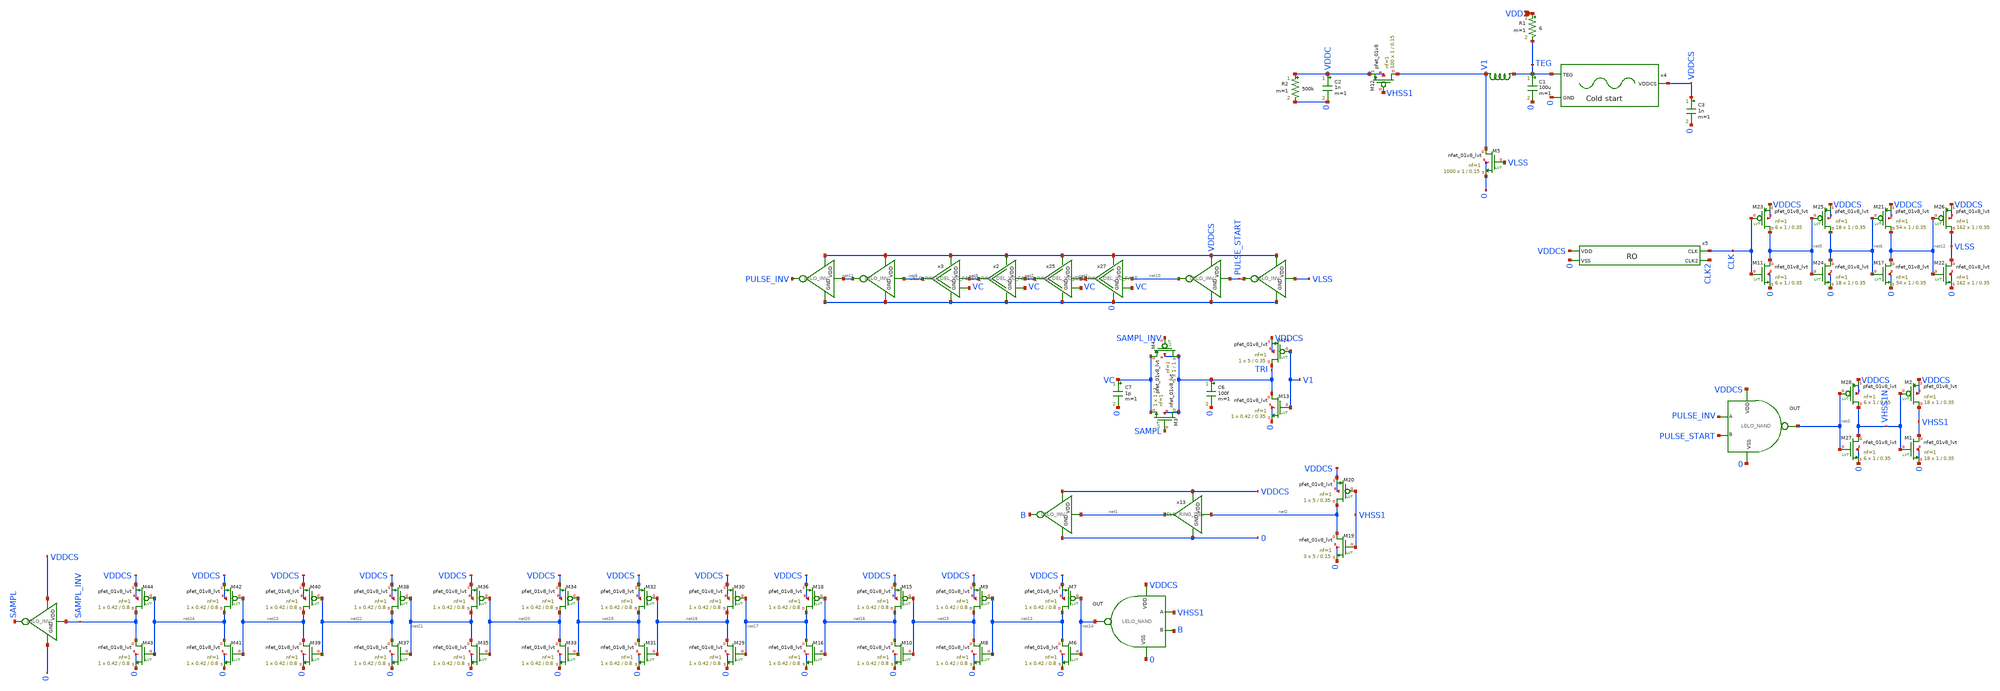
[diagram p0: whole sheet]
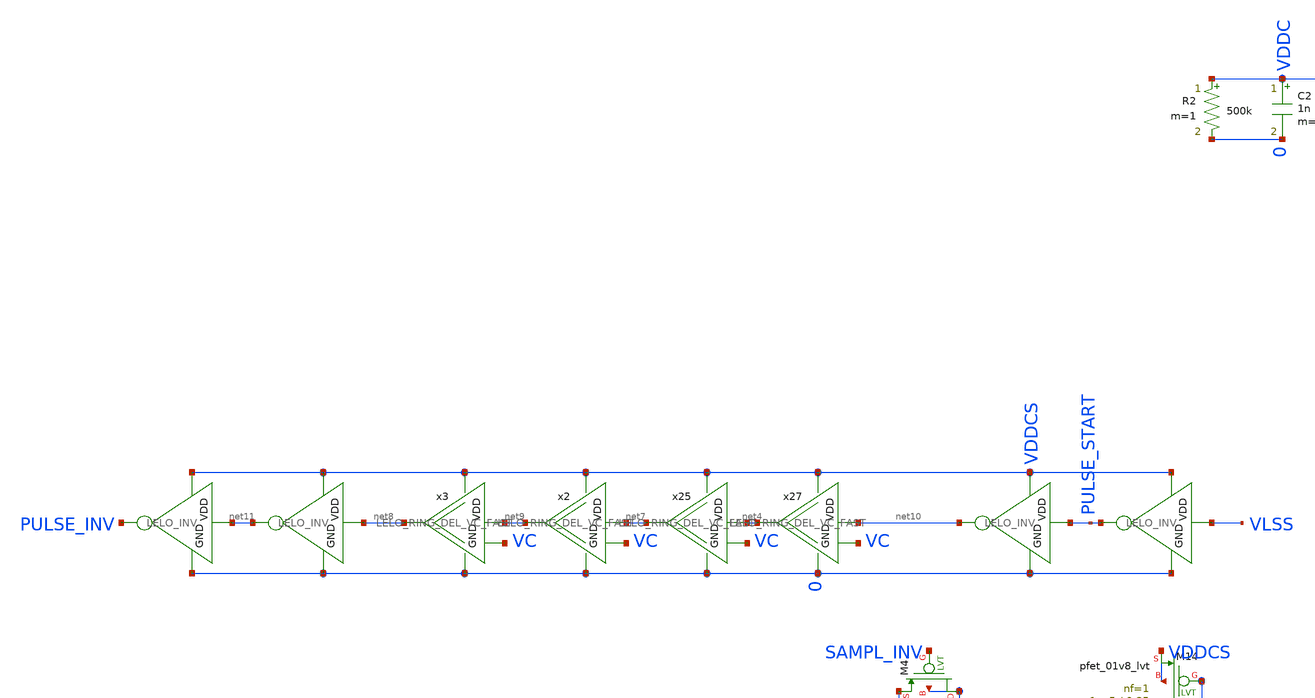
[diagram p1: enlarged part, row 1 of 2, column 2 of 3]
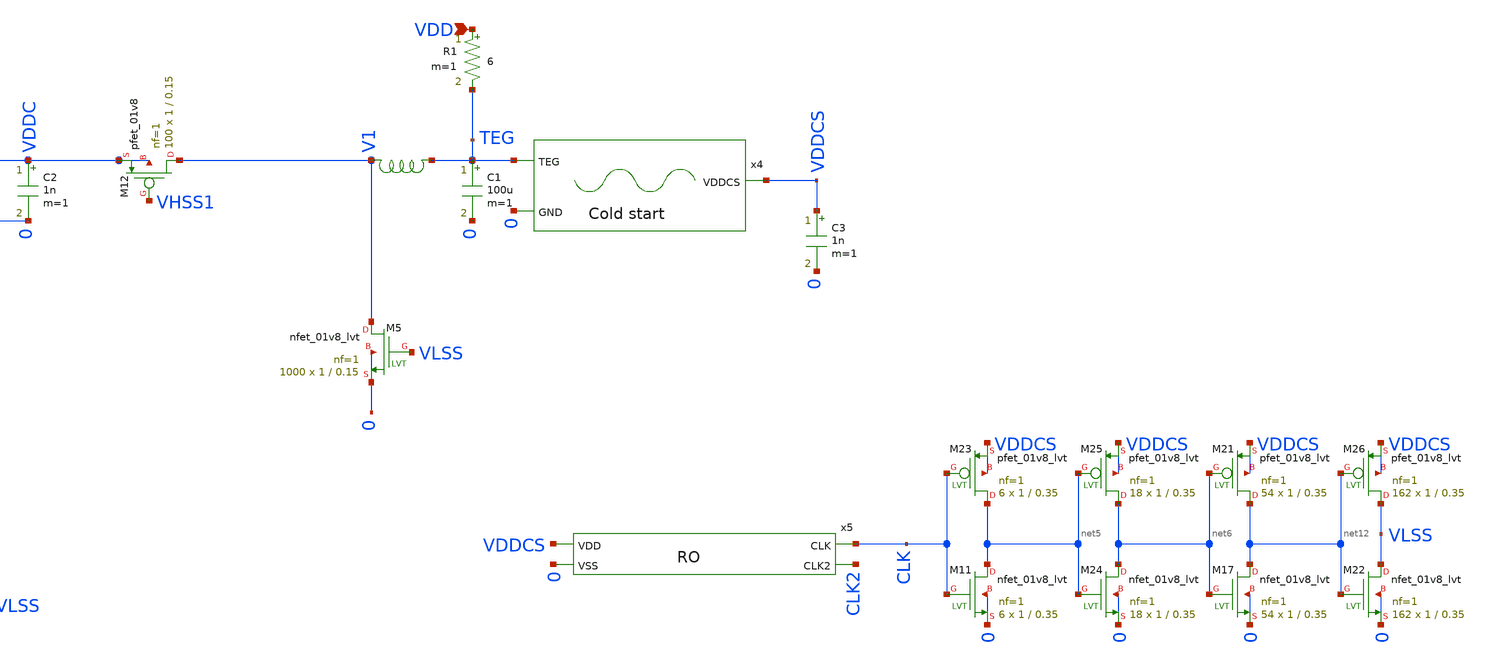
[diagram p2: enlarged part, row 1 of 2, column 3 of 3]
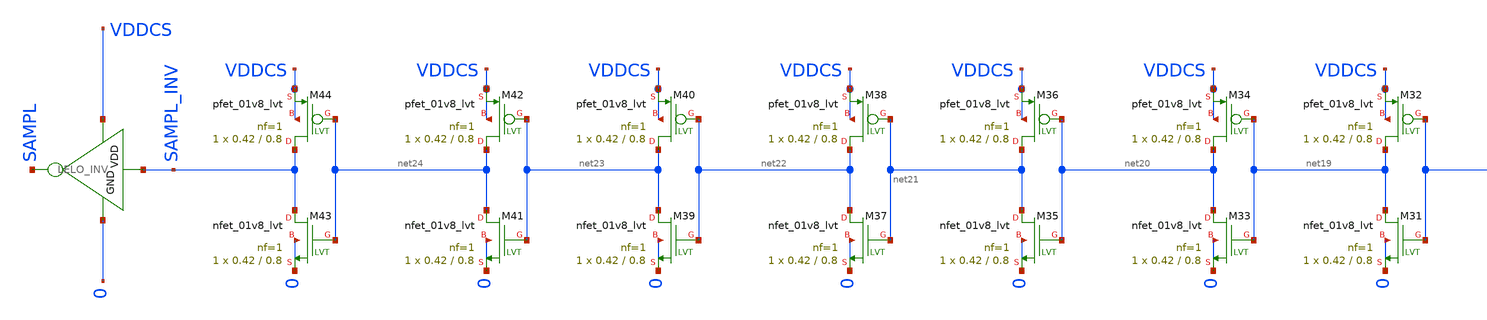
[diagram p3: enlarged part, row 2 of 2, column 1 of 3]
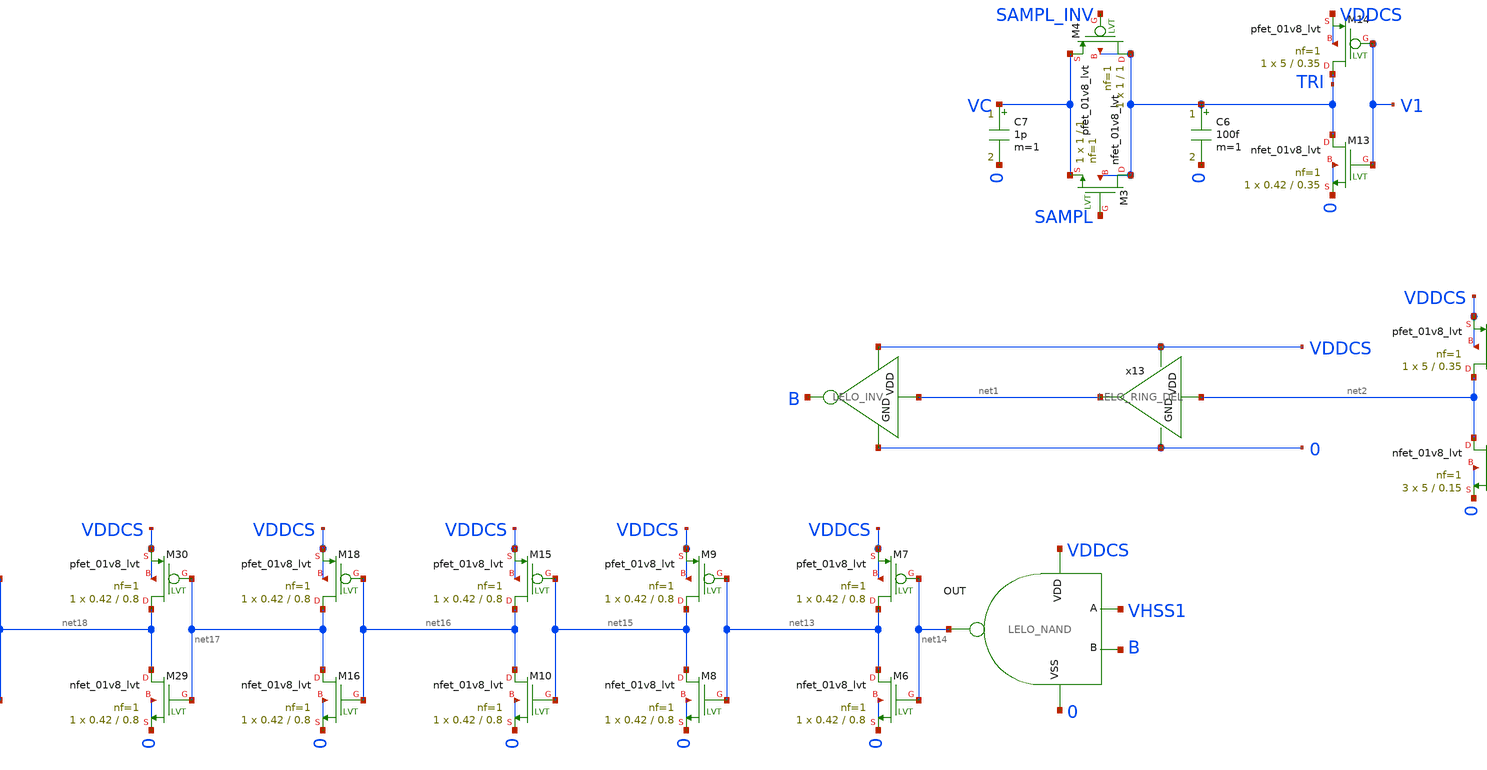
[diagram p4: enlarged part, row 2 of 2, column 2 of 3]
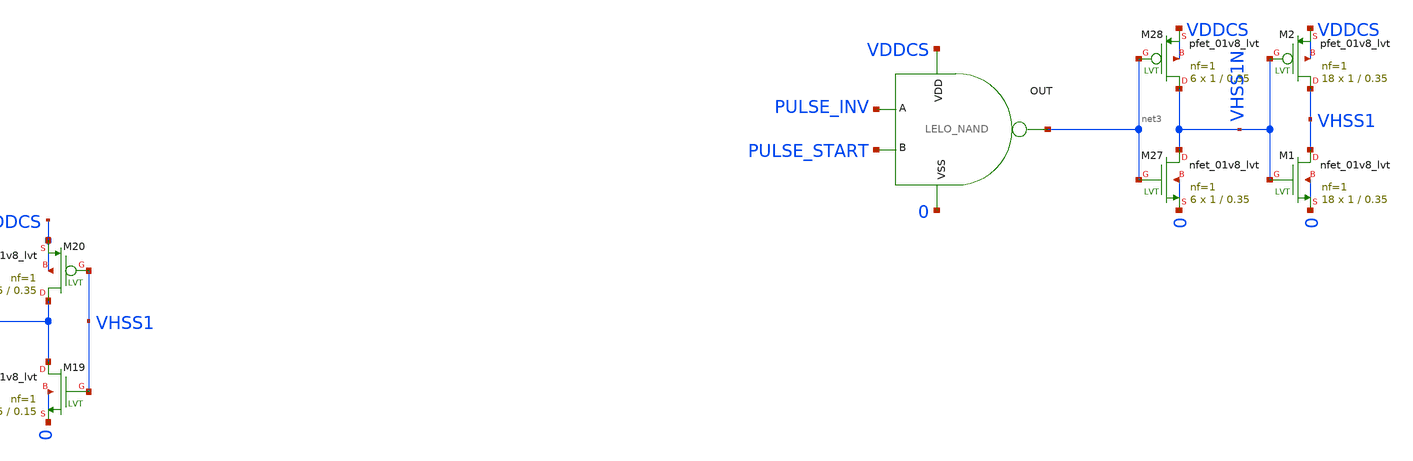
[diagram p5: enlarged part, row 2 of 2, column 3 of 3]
** sch_path: design/LELO_SVOD_SKY130A/LELO_EXSC.sch
**.subckt LELO_EXSC VDD
*.ipin VDD
R1 VDD TEG 6 m=1
XM13 TRI V1 0 0 sky130_fd_pr__nfet_01v8_lvt L=0.35 W=0.42 nf=1 ad='int((1 + 1)/2) * 0.42 / 1 * 0.29'
+ as='int((1 + 2)/2) * 0.42 / 1 * 0.29' pd='2*int((1 + 1)/2) * (0.42 / 1 + 0.29)' ps='2*int((1 + 2)/2) * (0.42 / 1 + 0.29)'
+ nrd='0.29 / 0.42 ' nrs='0.29 / 0.42 ' sa=0 sb=0 sd=0 mult=1 m=1
XM14 TRI V1 VDDCS VDDCS sky130_fd_pr__pfet_01v8_lvt L=0.35 W=5 nf=1 ad='int((1 + 1)/2) * 5 / 1 * 0.29'
+ as='int((1 + 2)/2) * 5 / 1 * 0.29' pd='2*int((1 + 1)/2) * (5 / 1 + 0.29)' ps='2*int((1 + 2)/2) * (5 / 1 + 0.29)'
+ nrd='0.29 / 5 ' nrs='0.29 / 5 ' sa=0 sb=0 sd=0 mult=1 m=1
C6 TRI 0 100f m=1
C7 VC 0 1p m=1
x13 VDDCS net2 net1 0 LELO_RING_DEL
x20 VDDCS net14 VHSS1 B 0 LELO_NAND
x22 VDDCS net1 B 0 LELO_INV
XM19 net2 VHSS1 0 0 sky130_fd_pr__nfet_01v8_lvt L=0.15 W=5 nf=1 ad='int((1 + 1)/2) * 5 / 1 * 0.29' as='int((1 + 2)/2) * 5 / 1 * 0.29'
+ pd='2*int((1 + 1)/2) * (5 / 1 + 0.29)' ps='2*int((1 + 2)/2) * (5 / 1 + 0.29)' nrd='0.29 / 5 ' nrs='0.29 / 5 '
+ sa=0 sb=0 sd=0 mult=3 m=3
XM20 net2 VHSS1 VDDCS VDDCS sky130_fd_pr__pfet_01v8_lvt L=0.35 W=5 nf=1 ad='int((1 + 1)/2) * 5 / 1 * 0.29'
+ as='int((1 + 2)/2) * 5 / 1 * 0.29' pd='2*int((1 + 1)/2) * (5 / 1 + 0.29)' ps='2*int((1 + 2)/2) * (5 / 1 + 0.29)'
+ nrd='0.29 / 5 ' nrs='0.29 / 5 ' sa=0 sb=0 sd=0 mult=1 m=1
x8 VDDCS net3 PULSE_INV PULSE_START 0 LELO_NAND
XM27 VHSS1N net3 0 0 sky130_fd_pr__nfet_01v8_lvt L=0.35 W=1 nf=1 ad='int((1 + 1)/2) * 1 / 1 * 0.29' as='int((1 + 2)/2) * 1 / 1 * 0.29'
+ pd='2*int((1 + 1)/2) * (1 / 1 + 0.29)' ps='2*int((1 + 2)/2) * (1 / 1 + 0.29)' nrd='0.29 / 1 ' nrs='0.29 / 1 '
+ sa=0 sb=0 sd=0 mult=6 m=6
XM28 VHSS1N net3 VDDCS VDDCS sky130_fd_pr__pfet_01v8_lvt L=0.35 W=1 nf=1 ad='int((1 + 1)/2) * 1 / 1 * 0.29'
+ as='int((1 + 2)/2) * 1 / 1 * 0.29' pd='2*int((1 + 1)/2) * (1 / 1 + 0.29)' ps='2*int((1 + 2)/2) * (1 / 1 + 0.29)'
+ nrd='0.29 / 1 ' nrs='0.29 / 1 ' sa=0 sb=0 sd=0 mult=6 m=6
x25 VDDCS net4 net7 0 VC LELO_RING_DEL_VC_FAST
x6 VDDCS net8 net11 0 LELO_INV
x27 VDDCS net10 net4 0 VC LELO_RING_DEL_VC_FAST
x5 VDDCS CLK CLK2 0 RO
XM11 net5 CLK 0 0 sky130_fd_pr__nfet_01v8_lvt L=0.35 W=1 nf=1 ad='int((1 + 1)/2) * 1 / 1 * 0.29' as='int((1 + 2)/2) * 1 / 1 * 0.29'
+ pd='2*int((1 + 1)/2) * (1 / 1 + 0.29)' ps='2*int((1 + 2)/2) * (1 / 1 + 0.29)' nrd='0.29 / 1 ' nrs='0.29 / 1 '
+ sa=0 sb=0 sd=0 mult=6 m=6
XM23 net5 CLK VDDCS VDDCS sky130_fd_pr__pfet_01v8_lvt L=0.35 W=1 nf=1 ad='int((1 + 1)/2) * 1 / 1 * 0.29'
+ as='int((1 + 2)/2) * 1 / 1 * 0.29' pd='2*int((1 + 1)/2) * (1 / 1 + 0.29)' ps='2*int((1 + 2)/2) * (1 / 1 + 0.29)'
+ nrd='0.29 / 1 ' nrs='0.29 / 1 ' sa=0 sb=0 sd=0 mult=6 m=6
XM24 net6 net5 0 0 sky130_fd_pr__nfet_01v8_lvt L=0.35 W=1 nf=1 ad='int((1 + 1)/2) * 1 / 1 * 0.29' as='int((1 + 2)/2) * 1 / 1 * 0.29'
+ pd='2*int((1 + 1)/2) * (1 / 1 + 0.29)' ps='2*int((1 + 2)/2) * (1 / 1 + 0.29)' nrd='0.29 / 1 ' nrs='0.29 / 1 '
+ sa=0 sb=0 sd=0 mult=18 m=18
XM25 net6 net5 VDDCS VDDCS sky130_fd_pr__pfet_01v8_lvt L=0.35 W=1 nf=1 ad='int((1 + 1)/2) * 1 / 1 * 0.29'
+ as='int((1 + 2)/2) * 1 / 1 * 0.29' pd='2*int((1 + 1)/2) * (1 / 1 + 0.29)' ps='2*int((1 + 2)/2) * (1 / 1 + 0.29)'
+ nrd='0.29 / 1 ' nrs='0.29 / 1 ' sa=0 sb=0 sd=0 mult=18 m=18
XM12 V1 VHSS1 VDDC VDDC sky130_fd_pr__pfet_01v8 L=0.15 W=1 nf=1 ad='int((1 + 1)/2) * 1 / 1 * 0.29' as='int((1 + 2)/2) * 1 / 1 * 0.29'
+ pd='2*int((1 + 1)/2) * (1 / 1 + 0.29)' ps='2*int((1 + 2)/2) * (1 / 1 + 0.29)' nrd='0.29 / 1 ' nrs='0.29 / 1 '
+ sa=0 sb=0 sd=0 mult=100 m=100
XM1 VHSS1 VHSS1N 0 0 sky130_fd_pr__nfet_01v8_lvt L=0.35 W=1 nf=1 ad='int((1 + 1)/2) * 1 / 1 * 0.29' as='int((1 + 2)/2) * 1 / 1 * 0.29'
+ pd='2*int((1 + 1)/2) * (1 / 1 + 0.29)' ps='2*int((1 + 2)/2) * (1 / 1 + 0.29)' nrd='0.29 / 1 ' nrs='0.29 / 1 '
+ sa=0 sb=0 sd=0 mult=18 m=18
XM2 VHSS1 VHSS1N VDDCS VDDCS sky130_fd_pr__pfet_01v8_lvt L=0.35 W=1 nf=1 ad='int((1 + 1)/2) * 1 / 1 * 0.29'
+ as='int((1 + 2)/2) * 1 / 1 * 0.29' pd='2*int((1 + 1)/2) * (1 / 1 + 0.29)' ps='2*int((1 + 2)/2) * (1 / 1 + 0.29)'
+ nrd='0.29 / 1 ' nrs='0.29 / 1 ' sa=0 sb=0 sd=0 mult=18 m=18
x2 VDDCS net7 net9 0 VC LELO_RING_DEL_VC_FAST
x3 VDDCS net9 net8 0 VC LELO_RING_DEL_VC_FAST
x1 VDDCS PULSE_START net10 0 LELO_INV
x16 VDDCS net11 PULSE_INV 0 LELO_INV
C1 TEG 0 100u m=1
x7 TEG V1 XGL6030-472_sat
x9 VDDCS VLSS PULSE_START 0 LELO_INV
XM5 V1 VLSS 0 0 sky130_fd_pr__nfet_01v8_lvt L=0.15 W=1 nf=1 ad='int((1 + 1)/2) * 1 / 1 * 0.29' as='int((1 + 2)/2) * 1 / 1 * 0.29'
+ pd='2*int((1 + 1)/2) * (1 / 1 + 0.29)' ps='2*int((1 + 2)/2) * (1 / 1 + 0.29)' nrd='0.29 / 1 ' nrs='0.29 / 1 '
+ sa=0 sb=0 sd=0 mult=1000 m=1000
XM17 net12 net6 0 0 sky130_fd_pr__nfet_01v8_lvt L=0.35 W=1 nf=1 ad='int((1 + 1)/2) * 1 / 1 * 0.29' as='int((1 + 2)/2) * 1 / 1 * 0.29'
+ pd='2*int((1 + 1)/2) * (1 / 1 + 0.29)' ps='2*int((1 + 2)/2) * (1 / 1 + 0.29)' nrd='0.29 / 1 ' nrs='0.29 / 1 '
+ sa=0 sb=0 sd=0 mult=54 m=54
XM21 net12 net6 VDDCS VDDCS sky130_fd_pr__pfet_01v8_lvt L=0.35 W=1 nf=1 ad='int((1 + 1)/2) * 1 / 1 * 0.29'
+ as='int((1 + 2)/2) * 1 / 1 * 0.29' pd='2*int((1 + 1)/2) * (1 / 1 + 0.29)' ps='2*int((1 + 2)/2) * (1 / 1 + 0.29)'
+ nrd='0.29 / 1 ' nrs='0.29 / 1 ' sa=0 sb=0 sd=0 mult=54 m=54
XM22 VLSS net12 0 0 sky130_fd_pr__nfet_01v8_lvt L=0.35 W=1 nf=1 ad='int((1 + 1)/2) * 1 / 1 * 0.29' as='int((1 + 2)/2) * 1 / 1 * 0.29'
+ pd='2*int((1 + 1)/2) * (1 / 1 + 0.29)' ps='2*int((1 + 2)/2) * (1 / 1 + 0.29)' nrd='0.29 / 1 ' nrs='0.29 / 1 '
+ sa=0 sb=0 sd=0 mult=162 m=162
XM26 VLSS net12 VDDCS VDDCS sky130_fd_pr__pfet_01v8_lvt L=0.35 W=1 nf=1 ad='int((1 + 1)/2) * 1 / 1 * 0.29'
+ as='int((1 + 2)/2) * 1 / 1 * 0.29' pd='2*int((1 + 1)/2) * (1 / 1 + 0.29)' ps='2*int((1 + 2)/2) * (1 / 1 + 0.29)'
+ nrd='0.29 / 1 ' nrs='0.29 / 1 ' sa=0 sb=0 sd=0 mult=162 m=162
C2 VDDC 0 1n m=1
R2 VDDC 0 500k m=1
x11 VDDCS SAMPL_INV SAMPL 0 LELO_INV
XM6 net13 net14 0 0 sky130_fd_pr__nfet_01v8_lvt L=0.8 W=0.42 nf=1 ad='int((1 + 1)/2) * 0.42 / 1 * 0.29'
+ as='int((1 + 2)/2) * 0.42 / 1 * 0.29' pd='2*int((1 + 1)/2) * (0.42 / 1 + 0.29)' ps='2*int((1 + 2)/2) * (0.42 / 1 + 0.29)'
+ nrd='0.29 / 0.42 ' nrs='0.29 / 0.42 ' sa=0 sb=0 sd=0 mult=1 m=1
XM7 net13 net14 VDDCS VDDCS sky130_fd_pr__pfet_01v8_lvt L=0.8 W=0.42 nf=1 ad='int((1 + 1)/2) * 0.42 / 1 * 0.29'
+ as='int((1 + 2)/2) * 0.42 / 1 * 0.29' pd='2*int((1 + 1)/2) * (0.42 / 1 + 0.29)' ps='2*int((1 + 2)/2) * (0.42 / 1 + 0.29)'
+ nrd='0.29 / 0.42 ' nrs='0.29 / 0.42 ' sa=0 sb=0 sd=0 mult=1 m=1
XM8 net15 net13 0 0 sky130_fd_pr__nfet_01v8_lvt L=0.8 W=0.42 nf=1 ad='int((1 + 1)/2) * 0.42 / 1 * 0.29'
+ as='int((1 + 2)/2) * 0.42 / 1 * 0.29' pd='2*int((1 + 1)/2) * (0.42 / 1 + 0.29)' ps='2*int((1 + 2)/2) * (0.42 / 1 + 0.29)'
+ nrd='0.29 / 0.42 ' nrs='0.29 / 0.42 ' sa=0 sb=0 sd=0 mult=1 m=1
XM9 net15 net13 VDDCS VDDCS sky130_fd_pr__pfet_01v8_lvt L=0.8 W=0.42 nf=1 ad='int((1 + 1)/2) * 0.42 / 1 * 0.29'
+ as='int((1 + 2)/2) * 0.42 / 1 * 0.29' pd='2*int((1 + 1)/2) * (0.42 / 1 + 0.29)' ps='2*int((1 + 2)/2) * (0.42 / 1 + 0.29)'
+ nrd='0.29 / 0.42 ' nrs='0.29 / 0.42 ' sa=0 sb=0 sd=0 mult=1 m=1
XM10 net16 net15 0 0 sky130_fd_pr__nfet_01v8_lvt L=0.8 W=0.42 nf=1 ad='int((1 + 1)/2) * 0.42 / 1 * 0.29'
+ as='int((1 + 2)/2) * 0.42 / 1 * 0.29' pd='2*int((1 + 1)/2) * (0.42 / 1 + 0.29)' ps='2*int((1 + 2)/2) * (0.42 / 1 + 0.29)'
+ nrd='0.29 / 0.42 ' nrs='0.29 / 0.42 ' sa=0 sb=0 sd=0 mult=1 m=1
XM15 net16 net15 VDDCS VDDCS sky130_fd_pr__pfet_01v8_lvt L=0.8 W=0.42 nf=1 ad='int((1 + 1)/2) * 0.42 / 1 * 0.29'
+ as='int((1 + 2)/2) * 0.42 / 1 * 0.29' pd='2*int((1 + 1)/2) * (0.42 / 1 + 0.29)' ps='2*int((1 + 2)/2) * (0.42 / 1 + 0.29)'
+ nrd='0.29 / 0.42 ' nrs='0.29 / 0.42 ' sa=0 sb=0 sd=0 mult=1 m=1
XM16 net17 net16 0 0 sky130_fd_pr__nfet_01v8_lvt L=0.8 W=0.42 nf=1 ad='int((1 + 1)/2) * 0.42 / 1 * 0.29'
+ as='int((1 + 2)/2) * 0.42 / 1 * 0.29' pd='2*int((1 + 1)/2) * (0.42 / 1 + 0.29)' ps='2*int((1 + 2)/2) * (0.42 / 1 + 0.29)'
+ nrd='0.29 / 0.42 ' nrs='0.29 / 0.42 ' sa=0 sb=0 sd=0 mult=1 m=1
XM18 net17 net16 VDDCS VDDCS sky130_fd_pr__pfet_01v8_lvt L=0.8 W=0.42 nf=1 ad='int((1 + 1)/2) * 0.42 / 1 * 0.29'
+ as='int((1 + 2)/2) * 0.42 / 1 * 0.29' pd='2*int((1 + 1)/2) * (0.42 / 1 + 0.29)' ps='2*int((1 + 2)/2) * (0.42 / 1 + 0.29)'
+ nrd='0.29 / 0.42 ' nrs='0.29 / 0.42 ' sa=0 sb=0 sd=0 mult=1 m=1
XM29 net18 net17 0 0 sky130_fd_pr__nfet_01v8_lvt L=0.8 W=0.42 nf=1 ad='int((1 + 1)/2) * 0.42 / 1 * 0.29'
+ as='int((1 + 2)/2) * 0.42 / 1 * 0.29' pd='2*int((1 + 1)/2) * (0.42 / 1 + 0.29)' ps='2*int((1 + 2)/2) * (0.42 / 1 + 0.29)'
+ nrd='0.29 / 0.42 ' nrs='0.29 / 0.42 ' sa=0 sb=0 sd=0 mult=1 m=1
XM30 net18 net17 VDDCS VDDCS sky130_fd_pr__pfet_01v8_lvt L=0.8 W=0.42 nf=1 ad='int((1 + 1)/2) * 0.42 / 1 * 0.29'
+ as='int((1 + 2)/2) * 0.42 / 1 * 0.29' pd='2*int((1 + 1)/2) * (0.42 / 1 + 0.29)' ps='2*int((1 + 2)/2) * (0.42 / 1 + 0.29)'
+ nrd='0.29 / 0.42 ' nrs='0.29 / 0.42 ' sa=0 sb=0 sd=0 mult=1 m=1
XM31 net19 net18 0 0 sky130_fd_pr__nfet_01v8_lvt L=0.8 W=0.42 nf=1 ad='int((1 + 1)/2) * 0.42 / 1 * 0.29'
+ as='int((1 + 2)/2) * 0.42 / 1 * 0.29' pd='2*int((1 + 1)/2) * (0.42 / 1 + 0.29)' ps='2*int((1 + 2)/2) * (0.42 / 1 + 0.29)'
+ nrd='0.29 / 0.42 ' nrs='0.29 / 0.42 ' sa=0 sb=0 sd=0 mult=1 m=1
XM32 net19 net18 VDDCS VDDCS sky130_fd_pr__pfet_01v8_lvt L=0.8 W=0.42 nf=1 ad='int((1 + 1)/2) * 0.42 / 1 * 0.29'
+ as='int((1 + 2)/2) * 0.42 / 1 * 0.29' pd='2*int((1 + 1)/2) * (0.42 / 1 + 0.29)' ps='2*int((1 + 2)/2) * (0.42 / 1 + 0.29)'
+ nrd='0.29 / 0.42 ' nrs='0.29 / 0.42 ' sa=0 sb=0 sd=0 mult=1 m=1
XM33 net20 net19 0 0 sky130_fd_pr__nfet_01v8_lvt L=0.8 W=0.42 nf=1 ad='int((1 + 1)/2) * 0.42 / 1 * 0.29'
+ as='int((1 + 2)/2) * 0.42 / 1 * 0.29' pd='2*int((1 + 1)/2) * (0.42 / 1 + 0.29)' ps='2*int((1 + 2)/2) * (0.42 / 1 + 0.29)'
+ nrd='0.29 / 0.42 ' nrs='0.29 / 0.42 ' sa=0 sb=0 sd=0 mult=1 m=1
XM34 net20 net19 VDDCS VDDCS sky130_fd_pr__pfet_01v8_lvt L=0.8 W=0.42 nf=1 ad='int((1 + 1)/2) * 0.42 / 1 * 0.29'
+ as='int((1 + 2)/2) * 0.42 / 1 * 0.29' pd='2*int((1 + 1)/2) * (0.42 / 1 + 0.29)' ps='2*int((1 + 2)/2) * (0.42 / 1 + 0.29)'
+ nrd='0.29 / 0.42 ' nrs='0.29 / 0.42 ' sa=0 sb=0 sd=0 mult=1 m=1
XM35 net21 net20 0 0 sky130_fd_pr__nfet_01v8_lvt L=0.8 W=0.42 nf=1 ad='int((1 + 1)/2) * 0.42 / 1 * 0.29'
+ as='int((1 + 2)/2) * 0.42 / 1 * 0.29' pd='2*int((1 + 1)/2) * (0.42 / 1 + 0.29)' ps='2*int((1 + 2)/2) * (0.42 / 1 + 0.29)'
+ nrd='0.29 / 0.42 ' nrs='0.29 / 0.42 ' sa=0 sb=0 sd=0 mult=1 m=1
XM36 net21 net20 VDDCS VDDCS sky130_fd_pr__pfet_01v8_lvt L=0.8 W=0.42 nf=1 ad='int((1 + 1)/2) * 0.42 / 1 * 0.29'
+ as='int((1 + 2)/2) * 0.42 / 1 * 0.29' pd='2*int((1 + 1)/2) * (0.42 / 1 + 0.29)' ps='2*int((1 + 2)/2) * (0.42 / 1 + 0.29)'
+ nrd='0.29 / 0.42 ' nrs='0.29 / 0.42 ' sa=0 sb=0 sd=0 mult=1 m=1
XM37 net22 net21 0 0 sky130_fd_pr__nfet_01v8_lvt L=0.8 W=0.42 nf=1 ad='int((1 + 1)/2) * 0.42 / 1 * 0.29'
+ as='int((1 + 2)/2) * 0.42 / 1 * 0.29' pd='2*int((1 + 1)/2) * (0.42 / 1 + 0.29)' ps='2*int((1 + 2)/2) * (0.42 / 1 + 0.29)'
+ nrd='0.29 / 0.42 ' nrs='0.29 / 0.42 ' sa=0 sb=0 sd=0 mult=1 m=1
XM38 net22 net21 VDDCS VDDCS sky130_fd_pr__pfet_01v8_lvt L=0.8 W=0.42 nf=1 ad='int((1 + 1)/2) * 0.42 / 1 * 0.29'
+ as='int((1 + 2)/2) * 0.42 / 1 * 0.29' pd='2*int((1 + 1)/2) * (0.42 / 1 + 0.29)' ps='2*int((1 + 2)/2) * (0.42 / 1 + 0.29)'
+ nrd='0.29 / 0.42 ' nrs='0.29 / 0.42 ' sa=0 sb=0 sd=0 mult=1 m=1
XM39 net23 net22 0 0 sky130_fd_pr__nfet_01v8_lvt L=0.8 W=0.42 nf=1 ad='int((1 + 1)/2) * 0.42 / 1 * 0.29'
+ as='int((1 + 2)/2) * 0.42 / 1 * 0.29' pd='2*int((1 + 1)/2) * (0.42 / 1 + 0.29)' ps='2*int((1 + 2)/2) * (0.42 / 1 + 0.29)'
+ nrd='0.29 / 0.42 ' nrs='0.29 / 0.42 ' sa=0 sb=0 sd=0 mult=1 m=1
XM40 net23 net22 VDDCS VDDCS sky130_fd_pr__pfet_01v8_lvt L=0.8 W=0.42 nf=1 ad='int((1 + 1)/2) * 0.42 / 1 * 0.29'
+ as='int((1 + 2)/2) * 0.42 / 1 * 0.29' pd='2*int((1 + 1)/2) * (0.42 / 1 + 0.29)' ps='2*int((1 + 2)/2) * (0.42 / 1 + 0.29)'
+ nrd='0.29 / 0.42 ' nrs='0.29 / 0.42 ' sa=0 sb=0 sd=0 mult=1 m=1
XM41 net24 net23 0 0 sky130_fd_pr__nfet_01v8_lvt L=0.8 W=0.42 nf=1 ad='int((1 + 1)/2) * 0.42 / 1 * 0.29'
+ as='int((1 + 2)/2) * 0.42 / 1 * 0.29' pd='2*int((1 + 1)/2) * (0.42 / 1 + 0.29)' ps='2*int((1 + 2)/2) * (0.42 / 1 + 0.29)'
+ nrd='0.29 / 0.42 ' nrs='0.29 / 0.42 ' sa=0 sb=0 sd=0 mult=1 m=1
XM42 net24 net23 VDDCS VDDCS sky130_fd_pr__pfet_01v8_lvt L=0.8 W=0.42 nf=1 ad='int((1 + 1)/2) * 0.42 / 1 * 0.29'
+ as='int((1 + 2)/2) * 0.42 / 1 * 0.29' pd='2*int((1 + 1)/2) * (0.42 / 1 + 0.29)' ps='2*int((1 + 2)/2) * (0.42 / 1 + 0.29)'
+ nrd='0.29 / 0.42 ' nrs='0.29 / 0.42 ' sa=0 sb=0 sd=0 mult=1 m=1
XM43 SAMPL_INV net24 0 0 sky130_fd_pr__nfet_01v8_lvt L=0.8 W=0.42 nf=1 ad='int((1 + 1)/2) * 0.42 / 1 * 0.29'
+ as='int((1 + 2)/2) * 0.42 / 1 * 0.29' pd='2*int((1 + 1)/2) * (0.42 / 1 + 0.29)' ps='2*int((1 + 2)/2) * (0.42 / 1 + 0.29)'
+ nrd='0.29 / 0.42 ' nrs='0.29 / 0.42 ' sa=0 sb=0 sd=0 mult=1 m=1
XM44 SAMPL_INV net24 VDDCS VDDCS sky130_fd_pr__pfet_01v8_lvt L=0.8 W=0.42 nf=1 ad='int((1 + 1)/2) * 0.42 / 1 * 0.29'
+ as='int((1 + 2)/2) * 0.42 / 1 * 0.29' pd='2*int((1 + 1)/2) * (0.42 / 1 + 0.29)' ps='2*int((1 + 2)/2) * (0.42 / 1 + 0.29)'
+ nrd='0.29 / 0.42 ' nrs='0.29 / 0.42 ' sa=0 sb=0 sd=0 mult=1 m=1
C3 VDDCS 0 1n m=1
x4 TEG VDDCS 0 LELO_COLD_START
XM3 TRI SAMPL VC TRI sky130_fd_pr__nfet_01v8_lvt L=1 W=1 nf=1 ad='int((1 + 1)/2) * 1 / 1 * 0.29' as='int((1 + 2)/2) * 1 / 1 * 0.29'
+ pd='2*int((1 + 1)/2) * (1 / 1 + 0.29)' ps='2*int((1 + 2)/2) * (1 / 1 + 0.29)' nrd='0.29 / 1 ' nrs='0.29 / 1 '
+ sa=0 sb=0 sd=0 mult=1 m=1
XM4 TRI SAMPL_INV VC TRI sky130_fd_pr__pfet_01v8_lvt L=1 W=1 nf=1 ad='int((1 + 1)/2) * 1 / 1 * 0.29'
+ as='int((1 + 2)/2) * 1 / 1 * 0.29' pd='2*int((1 + 1)/2) * (1 / 1 + 0.29)' ps='2*int((1 + 2)/2) * (1 / 1 + 0.29)'
+ nrd='0.29 / 1 ' nrs='0.29 / 1 ' sa=0 sb=0 sd=0 mult=1 m=1
**.ends

* expanding   symbol:  LELO_SVOD_SKY130A/LELO_RING_DEL.sym # of pins=4
** sym_path: design/LELO_SVOD_SKY130A/LELO_RING_DEL.sym
** sch_path: design/LELO_SVOD_SKY130A/LELO_RING_DEL.sch
.subckt LELO_RING_DEL VDD VIN VOUT GND
*.ipin VIN
*.ipin VDD
*.ipin GND
*.opin VOUT
XM1 VOUT VIN GND GND sky130_fd_pr__nfet_01v8_lvt L=1 W=0.42 nf=1 ad='int((1 + 1)/2) * 0.42 / 1 * 0.29'
+ as='int((1 + 2)/2) * 0.42 / 1 * 0.29' pd='2*int((1 + 1)/2) * (0.42 / 1 + 0.29)' ps='2*int((1 + 2)/2) * (0.42 / 1 + 0.29)'
+ nrd='0.29 / 0.42 ' nrs='0.29 / 0.42 ' sa=0 sb=0 sd=0 mult=1 m=1
XM2 VOUT VIN VDD VDD sky130_fd_pr__pfet_01v8_lvt L=1 W=0.42 nf=1 ad='int((1 + 1)/2) * 0.42 / 1 * 0.29'
+ as='int((1 + 2)/2) * 0.42 / 1 * 0.29' pd='2*int((1 + 1)/2) * (0.42 / 1 + 0.29)' ps='2*int((1 + 2)/2) * (0.42 / 1 + 0.29)'
+ nrd='0.29 / 0.42 ' nrs='0.29 / 0.42 ' sa=0 sb=0 sd=0 mult=1 m=1
.ends


* expanding   symbol:  LELO_SVOD_SKY130A/LELO_NAND.sym # of pins=5
** sym_path: design/LELO_SVOD_SKY130A/LELO_NAND.sym
** sch_path: design/LELO_SVOD_SKY130A/LELO_NAND.sch
.subckt LELO_NAND VDD OUT A B VSS
*.ipin VDD
*.ipin VSS
*.opin OUT
*.ipin A
*.ipin B
XM1 net1 A VSS VSS sky130_fd_pr__nfet_01v8_lvt L=0.15 W=1 nf=1 ad='int((1 + 1)/2) * 1 / 1 * 0.29' as='int((1 + 2)/2) * 1 / 1 * 0.29'
+ pd='2*int((1 + 1)/2) * (1 / 1 + 0.29)' ps='2*int((1 + 2)/2) * (1 / 1 + 0.29)' nrd='0.29 / 1 ' nrs='0.29 / 1 '
+ sa=0 sb=0 sd=0 mult=1 m=1
XM2 OUT B net1 net1 sky130_fd_pr__nfet_01v8_lvt L=0.15 W=1 nf=1 ad='int((1 + 1)/2) * 1 / 1 * 0.29' as='int((1 + 2)/2) * 1 / 1 * 0.29'
+ pd='2*int((1 + 1)/2) * (1 / 1 + 0.29)' ps='2*int((1 + 2)/2) * (1 / 1 + 0.29)' nrd='0.29 / 1 ' nrs='0.29 / 1 '
+ sa=0 sb=0 sd=0 mult=1 m=1
XM3 OUT A VDD VDD sky130_fd_pr__pfet_01v8_lvt L=0.35 W=1 nf=1 ad='int((1 + 1)/2) * 1 / 1 * 0.29' as='int((1 + 2)/2) * 1 / 1 * 0.29'
+ pd='2*int((1 + 1)/2) * (1 / 1 + 0.29)' ps='2*int((1 + 2)/2) * (1 / 1 + 0.29)' nrd='0.29 / 1 ' nrs='0.29 / 1 '
+ sa=0 sb=0 sd=0 mult=1 m=1
XM4 OUT B VDD VDD sky130_fd_pr__pfet_01v8_lvt L=0.35 W=1 nf=1 ad='int((1 + 1)/2) * 1 / 1 * 0.29' as='int((1 + 2)/2) * 1 / 1 * 0.29'
+ pd='2*int((1 + 1)/2) * (1 / 1 + 0.29)' ps='2*int((1 + 2)/2) * (1 / 1 + 0.29)' nrd='0.29 / 1 ' nrs='0.29 / 1 '
+ sa=0 sb=0 sd=0 mult=1 m=1
.ends


* expanding   symbol:  LELO_SVOD_SKY130A/LELO_INV.sym # of pins=4
** sym_path: design/LELO_SVOD_SKY130A/LELO_INV.sym
** sch_path: design/LELO_SVOD_SKY130A/LELO_INV.sch
.subckt LELO_INV VDD VIN VOUT GND
*.ipin VIN
*.ipin VDD
*.ipin GND
*.opin VOUT
XM1 VOUT VIN GND GND sky130_fd_pr__nfet_01v8_lvt L=0.15 W=1 nf=1 ad='int((1 + 1)/2) * 1 / 1 * 0.29' as='int((1 + 2)/2) * 1 / 1 * 0.29'
+ pd='2*int((1 + 1)/2) * (1 / 1 + 0.29)' ps='2*int((1 + 2)/2) * (1 / 1 + 0.29)' nrd='0.29 / 1 ' nrs='0.29 / 1 '
+ sa=0 sb=0 sd=0 mult=1 m=1
XM2 VOUT VIN VDD VDD sky130_fd_pr__pfet_01v8_lvt L=0.35 W=1 nf=1 ad='int((1 + 1)/2) * 1 / 1 * 0.29' as='int((1 + 2)/2) * 1 / 1 * 0.29'
+ pd='2*int((1 + 1)/2) * (1 / 1 + 0.29)' ps='2*int((1 + 2)/2) * (1 / 1 + 0.29)' nrd='0.29 / 1 ' nrs='0.29 / 1 '
+ sa=0 sb=0 sd=0 mult=2 m=2
.ends


* expanding   symbol:  LELO_SVOD_SKY130A/LELO_RING_DEL_VC_FAST.sym # of pins=5
** sym_path: design/LELO_SVOD_SKY130A/LELO_RING_DEL_VC_FAST.sym
** sch_path: design/LELO_SVOD_SKY130A/LELO_RING_DEL_VC_FAST.sch
.subckt LELO_RING_DEL_VC_FAST VDD VIN VOUT GND VC
*.ipin VIN
*.ipin VDD
*.opin VOUT
*.ipin VC
*.ipin GND
XM1 VOUT VIN net1 GND sky130_fd_pr__nfet_01v8_lvt L=0.15 W=3 nf=1 ad='int((1 + 1)/2) * 3 / 1 * 0.29'
+ as='int((1 + 2)/2) * 3 / 1 * 0.29' pd='2*int((1 + 1)/2) * (3 / 1 + 0.29)' ps='2*int((1 + 2)/2) * (3 / 1 + 0.29)'
+ nrd='0.29 / 3 ' nrs='0.29 / 3 ' sa=0 sb=0 sd=0 mult=1 m=1
XM2 VOUT VIN VDD VDD sky130_fd_pr__pfet_01v8_lvt L=2 W=0.42 nf=1 ad='int((1 + 1)/2) * 0.42 / 1 * 0.29'
+ as='int((1 + 2)/2) * 0.42 / 1 * 0.29' pd='2*int((1 + 1)/2) * (0.42 / 1 + 0.29)' ps='2*int((1 + 2)/2) * (0.42 / 1 + 0.29)'
+ nrd='0.29 / 0.42 ' nrs='0.29 / 0.42 ' sa=0 sb=0 sd=0 mult=1 m=1
XM3 net1 VIN GND GND sky130_fd_pr__nfet_01v8_lvt L=10 W=0.42 nf=1 ad='int((1 + 1)/2) * 0.42 / 1 * 0.29'
+ as='int((1 + 2)/2) * 0.42 / 1 * 0.29' pd='2*int((1 + 1)/2) * (0.42 / 1 + 0.29)' ps='2*int((1 + 2)/2) * (0.42 / 1 + 0.29)'
+ nrd='0.29 / 0.42 ' nrs='0.29 / 0.42 ' sa=0 sb=0 sd=0 mult=1 m=1
XM4 net1 VC GND GND sky130_fd_pr__nfet_01v8 L=0.15 W=6 nf=1 ad='int((1 + 1)/2) * 6 / 1 * 0.29' as='int((1 + 2)/2) * 6 / 1 * 0.29'
+ pd='2*int((1 + 1)/2) * (6 / 1 + 0.29)' ps='2*int((1 + 2)/2) * (6 / 1 + 0.29)' nrd='0.29 / 6 ' nrs='0.29 / 6 '
+ sa=0 sb=0 sd=0 mult=1 m=1
.ends


* expanding   symbol:  LELO_SVOD_SKY130A/RO.sym # of pins=4
** sym_path: design/LELO_SVOD_SKY130A/RO.sym
** sch_path: design/LELO_SVOD_SKY130A/RO.sch
.subckt RO VDD CLK CLK2 VSS
*.opin CLK
*.ipin VSS
*.opin CLK2
*.ipin VDD
x1 VDD CLK net1 VSS CLK LELO_RING_DEL_VC
x2 VDD net1 CLK2 VSS net1 LELO_RING_DEL_VC
x3 VDD CLK2 net3 VSS CLK2 LELO_RING_DEL_VC
x4 VDD net3 net2 VSS net3 LELO_RING_DEL_VC
x5 VDD net2 CLK VSS net2 LELO_RING_DEL_VC
.ends


* expanding   symbol:  LELO_SVOD_SKY130A/XGL6030-472_sat.sym # of pins=2
** sym_path: design/LELO_SVOD_SKY130A/XGL6030-472_sat.sym

.subckt XGL6030-472_sat port1 port2
X1 port1 port2 Model1C R1=5 R2=0.021 C=13.9p K1=0.000001 K2=1.05 K3= 4.7u K4=0.000001 K5=0.000001
+ L=4.5383E-06 Is=18.1418 a=0.725 L_Z0=0 L_EL=0 L_F0=0E6 PkZ=4358.77183
.ends XGL6030-472_sat


* expanding   symbol:  LELO_SVOD_SKY130A/LELO_COLD_START.sym # of pins=3
** sym_path: design/LELO_SVOD_SKY130A/LELO_COLD_START.sym
** sch_path: design/LELO_SVOD_SKY130A/LELO_COLD_START.sch
.subckt LELO_COLD_START TEG VDDCS GND
*.ipin GND
*.ipin TEG
*.opin VDDCS
C2 VG2 net4 110p m=1
x1 VG2 net2 1812PS-564_imp
x2 net1 VG1 1812PS-564_imp
C4 VG1 net3 110p m=1
XM1 net1 VG2 GND GND sky130_fd_pr__nfet_20v0_zvt W=60 L=0.5 m=100
XM2 net2 VG1 GND GND sky130_fd_pr__nfet_20v0_zvt W=60 L=0.5 m=100
XM3 TEG TEG net4 TEG sky130_fd_pr__nfet_01v8_lvt L=0.15 W=10 nf=1 ad='int((1 + 1)/2) * 10 / 1 * 0.29'
+ as='int((1 + 2)/2) * 10 / 1 * 0.29' pd='2*int((1 + 1)/2) * (10 / 1 + 0.29)' ps='2*int((1 + 2)/2) * (10 / 1 + 0.29)'
+ nrd='0.29 / 10 ' nrs='0.29 / 10 ' sa=0 sb=0 sd=0 mult=1 m=1
XM7 net4 net4 net3 net4 sky130_fd_pr__nfet_01v8_lvt L=0.15 W=10 nf=1 ad='int((1 + 1)/2) * 10 / 1 * 0.29'
+ as='int((1 + 2)/2) * 10 / 1 * 0.29' pd='2*int((1 + 1)/2) * (10 / 1 + 0.29)' ps='2*int((1 + 2)/2) * (10 / 1 + 0.29)'
+ nrd='0.29 / 10 ' nrs='0.29 / 10 ' sa=0 sb=0 sd=0 mult=1 m=1
XM8 net3 net3 VDDCS net3 sky130_fd_pr__nfet_01v8_lvt L=0.15 W=10 nf=1 ad='int((1 + 1)/2) * 10 / 1 * 0.29'
+ as='int((1 + 2)/2) * 10 / 1 * 0.29' pd='2*int((1 + 1)/2) * (10 / 1 + 0.29)' ps='2*int((1 + 2)/2) * (10 / 1 + 0.29)'
+ nrd='0.29 / 10 ' nrs='0.29 / 10 ' sa=0 sb=0 sd=0 mult=1 m=1
x3 TEG net2 XGL6030-472_sat
x4 TEG net1 XGL6030-472_sat
.ends


* expanding   symbol:  LELO_SVOD_SKY130A/LELO_RING_DEL_VC.sym # of pins=5
** sym_path: design/LELO_SVOD_SKY130A/LELO_RING_DEL_VC.sym
** sch_path: design/LELO_SVOD_SKY130A/LELO_RING_DEL_VC.sch
.subckt LELO_RING_DEL_VC VDD VIN VOUT GND VC
*.ipin VIN
*.ipin VDD
*.ipin GND
*.opin VOUT
*.ipin VC
XM1 VOUT VIN net1 GND sky130_fd_pr__nfet_01v8_lvt L=0.15 W=0.42 nf=1 ad='int((1 + 1)/2) * 0.42 / 1 * 0.29'
+ as='int((1 + 2)/2) * 0.42 / 1 * 0.29' pd='2*int((1 + 1)/2) * (0.42 / 1 + 0.29)' ps='2*int((1 + 2)/2) * (0.42 / 1 + 0.29)'
+ nrd='0.29 / 0.42 ' nrs='0.29 / 0.42 ' sa=0 sb=0 sd=0 mult=1 m=1
XM2 VOUT VIN VDD VDD sky130_fd_pr__pfet_01v8_lvt L=3 W=0.42 nf=1 ad='int((1 + 1)/2) * 0.42 / 1 * 0.29'
+ as='int((1 + 2)/2) * 0.42 / 1 * 0.29' pd='2*int((1 + 1)/2) * (0.42 / 1 + 0.29)' ps='2*int((1 + 2)/2) * (0.42 / 1 + 0.29)'
+ nrd='0.29 / 0.42 ' nrs='0.29 / 0.42 ' sa=0 sb=0 sd=0 mult=1 m=1
XM3 net1 VIN GND GND sky130_fd_pr__nfet_01v8_lvt L=4 W=0.42 nf=1 ad='int((1 + 1)/2) * 0.42 / 1 * 0.29'
+ as='int((1 + 2)/2) * 0.42 / 1 * 0.29' pd='2*int((1 + 1)/2) * (0.42 / 1 + 0.29)' ps='2*int((1 + 2)/2) * (0.42 / 1 + 0.29)'
+ nrd='0.29 / 0.42 ' nrs='0.29 / 0.42 ' sa=0 sb=0 sd=0 mult=1 m=1
XM4 net1 VC GND GND sky130_fd_pr__nfet_01v8_lvt L=4 W=0.42 nf=1 ad='int((1 + 1)/2) * 0.42 / 1 * 0.29'
+ as='int((1 + 2)/2) * 0.42 / 1 * 0.29' pd='2*int((1 + 1)/2) * (0.42 / 1 + 0.29)' ps='2*int((1 + 2)/2) * (0.42 / 1 + 0.29)'
+ nrd='0.29 / 0.42 ' nrs='0.29 / 0.42 ' sa=0 sb=0 sd=0 mult=1 m=1
.ends


* expanding   symbol:  LELO_SVOD_SKY130A/1812PS-564_imp.sym # of pins=2
** sym_path: design/LELO_SVOD_SKY130A/1812PS-564_imp.sym

.subckt 1812PS-564_imp port1 port2
X1 port1 port2 Model1D R1=70 R2=6.1 C= 7.71p K1=0.000001 K2=115.8 K3= 560u K4=0.000001 K5=0.000001
+ L=0 Is=0 a=0 L_Z0=0 L_EL=0 L_F0=0E6 PkZ=153558.837
.ends 1812PS-564_imp
.end
